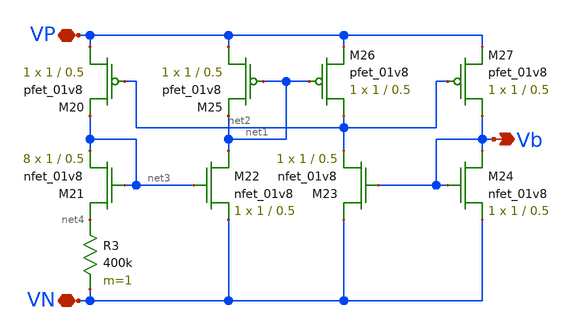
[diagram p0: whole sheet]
** sch_path: dac/schematics/bias_generator.sch
**.subckt bias_generator VP VN Vb
*.iopin VP
*.iopin VN
*.opin Vb
XM20 VP net2 net3 VDD sky130_fd_pr__pfet_01v8 L=0.5 W=1 nf=1 ad='int((nf+1)/2) * W/nf * 0.29' as='int((nf+2)/2) * W/nf * 0.29'
+ pd='2*int((nf+1)/2) * (W/nf + 0.29)' ps='2*int((nf+2)/2) * (W/nf + 0.29)' nrd='0.29 / W' nrs='0.29 / W'
+ sa=0 sb=0 sd=0 mult=1 m=1
XM21 net4 net3 net3 GND sky130_fd_pr__nfet_01v8 L=0.5 W=1 nf=1 ad='int((nf+1)/2) * W/nf * 0.29' as='int((nf+2)/2) * W/nf * 0.29'
+ pd='2*int((nf+1)/2) * (W/nf + 0.29)' ps='2*int((nf+2)/2) * (W/nf + 0.29)' nrd='0.29 / W' nrs='0.29 / W'
+ sa=0 sb=0 sd=0 mult=8 m=8
R3 net4 VN 400k m=1
XM22 net1 net3 VN GND sky130_fd_pr__nfet_01v8 L=0.5 W=1 nf=1 ad='int((nf+1)/2) * W/nf * 0.29' as='int((nf+2)/2) * W/nf * 0.29'
+ pd='2*int((nf+1)/2) * (W/nf + 0.29)' ps='2*int((nf+2)/2) * (W/nf + 0.29)' nrd='0.29 / W' nrs='0.29 / W'
+ sa=0 sb=0 sd=0 mult=1 m=1
XM23 VN Vb net2 GND sky130_fd_pr__nfet_01v8 L=0.5 W=1 nf=1 ad='int((nf+1)/2) * W/nf * 0.29' as='int((nf+2)/2) * W/nf * 0.29'
+ pd='2*int((nf+1)/2) * (W/nf + 0.29)' ps='2*int((nf+2)/2) * (W/nf + 0.29)' nrd='0.29 / W' nrs='0.29 / W'
+ sa=0 sb=0 sd=0 mult=1 m=1
XM24 Vb Vb VN GND sky130_fd_pr__nfet_01v8 L=0.5 W=1 nf=1 ad='int((nf+1)/2) * W/nf * 0.29' as='int((nf+2)/2) * W/nf * 0.29'
+ pd='2*int((nf+1)/2) * (W/nf + 0.29)' ps='2*int((nf+2)/2) * (W/nf + 0.29)' nrd='0.29 / W' nrs='0.29 / W'
+ sa=0 sb=0 sd=0 mult=1 m=1
XM25 VP net1 net1 VDD sky130_fd_pr__pfet_01v8 L=0.5 W=1 nf=1 ad='int((nf+1)/2) * W/nf * 0.29' as='int((nf+2)/2) * W/nf * 0.29'
+ pd='2*int((nf+1)/2) * (W/nf + 0.29)' ps='2*int((nf+2)/2) * (W/nf + 0.29)' nrd='0.29 / W' nrs='0.29 / W'
+ sa=0 sb=0 sd=0 mult=1 m=1
XM26 net2 net1 VP VDD sky130_fd_pr__pfet_01v8 L=0.5 W=1 nf=1 ad='int((nf+1)/2) * W/nf * 0.29' as='int((nf+2)/2) * W/nf * 0.29'
+ pd='2*int((nf+1)/2) * (W/nf + 0.29)' ps='2*int((nf+2)/2) * (W/nf + 0.29)' nrd='0.29 / W' nrs='0.29 / W'
+ sa=0 sb=0 sd=0 mult=1 m=1
XM27 Vb net2 VP VDD sky130_fd_pr__pfet_01v8 L=0.5 W=1 nf=1 ad='int((nf+1)/2) * W/nf * 0.29' as='int((nf+2)/2) * W/nf * 0.29'
+ pd='2*int((nf+1)/2) * (W/nf + 0.29)' ps='2*int((nf+2)/2) * (W/nf + 0.29)' nrd='0.29 / W' nrs='0.29 / W'
+ sa=0 sb=0 sd=0 mult=1 m=1
**.ends
.end
